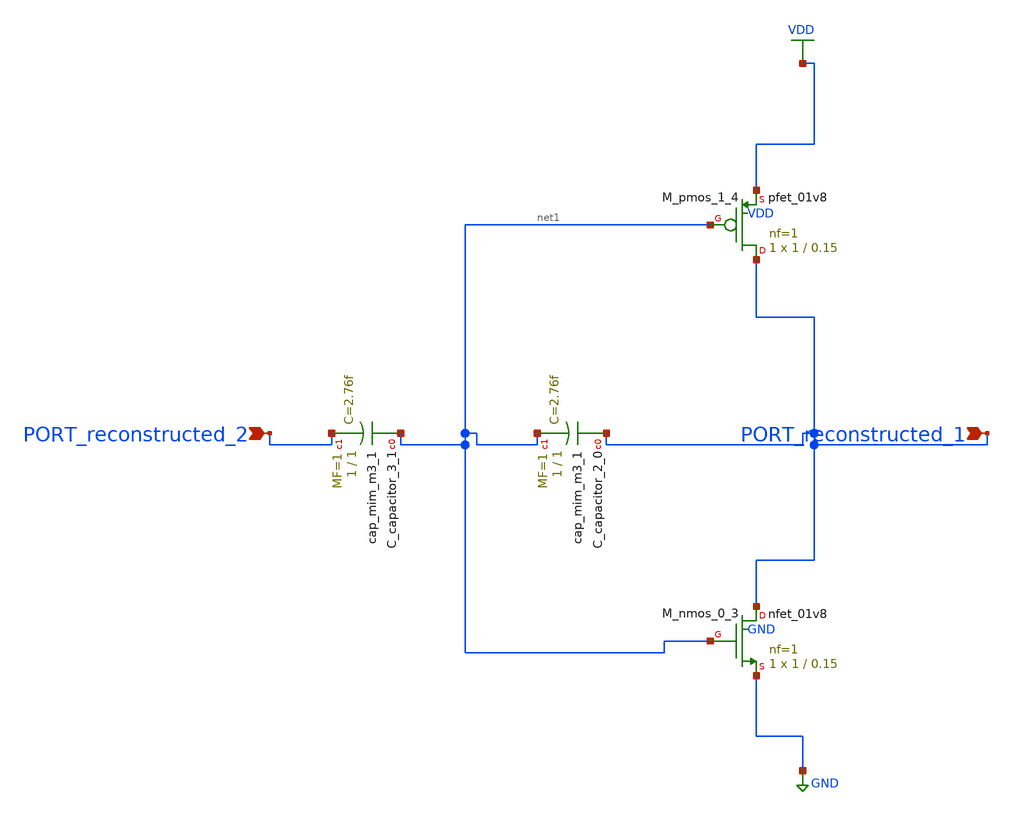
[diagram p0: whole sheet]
** sch_path: schematics/AMSNet/613.sch
**.subckt 613 PORT_reconstructed_1 PORT_reconstructed_2
*.ipin PORT_reconstructed_1
*.ipin PORT_reconstructed_2
XC_capacitor_2_0 PORT_reconstructed_1 net1 sky130_fd_pr__cap_mim_m3_1 W=1 L=1 MF=1 m=1
XC_capacitor_3_1 net1 PORT_reconstructed_2 sky130_fd_pr__cap_mim_m3_1 W=1 L=1 MF=1 m=1
XM_nmos_0_3 PORT_reconstructed_1 net1 GND GND sky130_fd_pr__nfet_01v8 L=0.15 W=1 nf=1 ad='int((1 + 1)/2) * 1 / 1 * 0.29'
+ as='int((1 + 2)/2) * 1 / 1 * 0.29' pd='2*int((1 + 1)/2) * (1 / 1 + 0.29)' ps='2*int((1 + 2)/2) * (1 / 1 + 0.29)'
+ nrd='0.29 / 1 ' nrs='0.29 / 1 ' sa=0 sb=0 sd=0 mult=1 m=1
XM_pmos_1_4 PORT_reconstructed_1 net1 VDD VDD sky130_fd_pr__pfet_01v8 L=0.15 W=1 nf=1 ad='int((1 + 1)/2) * 1 / 1 * 0.29'
+ as='int((1 + 2)/2) * 1 / 1 * 0.29' pd='2*int((1 + 1)/2) * (1 / 1 + 0.29)' ps='2*int((1 + 2)/2) * (1 / 1 + 0.29)'
+ nrd='0.29 / 1 ' nrs='0.29 / 1 ' sa=0 sb=0 sd=0 mult=1 m=1
**.ends
.GLOBAL GND
.GLOBAL VDD
.end
